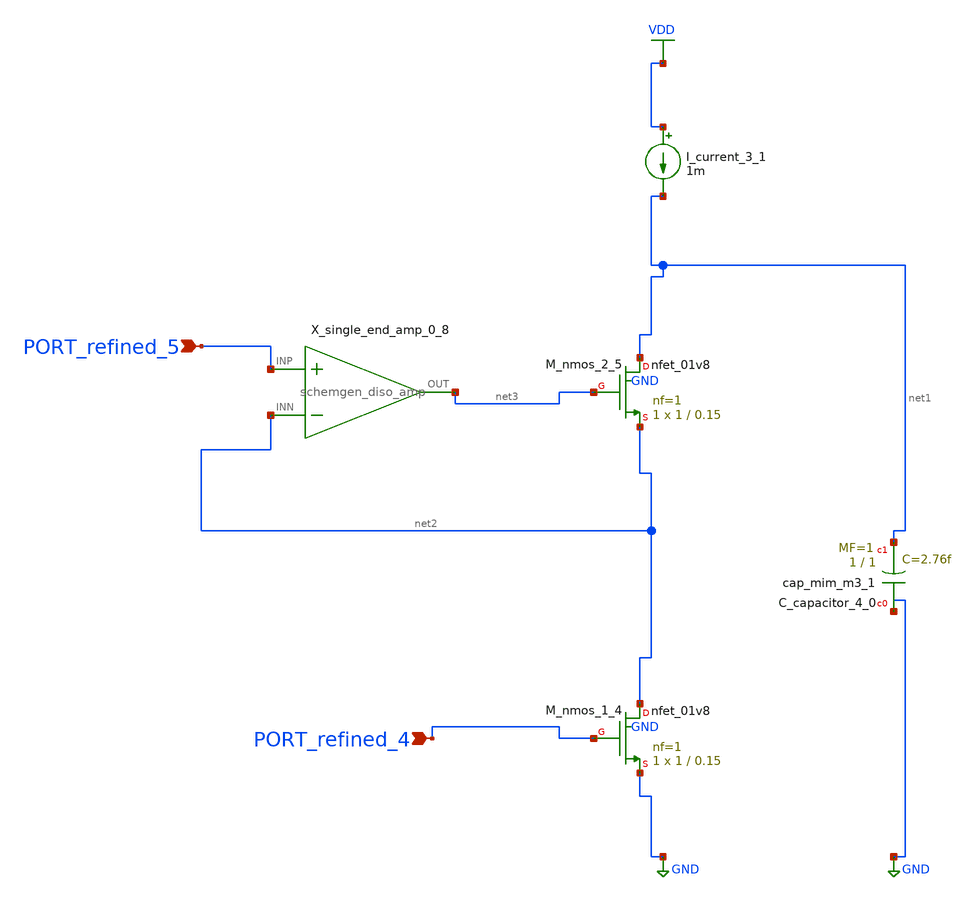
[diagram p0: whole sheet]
** sch_path: schematics/Image2Net/090.sch
**.subckt 090 PORT_refined_4 PORT_refined_5
*.ipin PORT_refined_4
*.ipin PORT_refined_5
XC_capacitor_4_0 GND net1 sky130_fd_pr__cap_mim_m3_1 W=1 L=1 MF=1 m=1
I_current_3_1 VDD net1 1m
XM_nmos_1_4 net2 PORT_refined_4 GND GND sky130_fd_pr__nfet_01v8 L=0.15 W=1 nf=1 ad='int((1 + 1)/2) * 1 / 1 * 0.29'
+ as='int((1 + 2)/2) * 1 / 1 * 0.29' pd='2*int((1 + 1)/2) * (1 / 1 + 0.29)' ps='2*int((1 + 2)/2) * (1 / 1 + 0.29)'
+ nrd='0.29 / 1 ' nrs='0.29 / 1 ' sa=0 sb=0 sd=0 mult=1 m=1
XM_nmos_2_5 net1 net3 net2 GND sky130_fd_pr__nfet_01v8 L=0.15 W=1 nf=1 ad='int((1 + 1)/2) * 1 / 1 * 0.29'
+ as='int((1 + 2)/2) * 1 / 1 * 0.29' pd='2*int((1 + 1)/2) * (1 / 1 + 0.29)' ps='2*int((1 + 2)/2) * (1 / 1 + 0.29)'
+ nrd='0.29 / 1 ' nrs='0.29 / 1 ' sa=0 sb=0 sd=0 mult=1 m=1
X_single_end_amp_0_8 PORT_refined_5 net2 net3 schemgen_diso_amp
**.ends

* expanding   symbol:  schemgen_diso_amp.sym # of pins=3
** sym_path: symbols/schemgen_diso_amp.sym
.subckt schemgen_diso_amp INP INN OUT
* SchemGen ideal op-amp: Vout = 1e5 * (V(INP) - V(INN))
E1 OUT 0 INP INN 1e5
.ends schemgen_diso_amp
.GLOBAL GND
.GLOBAL VDD
.end
